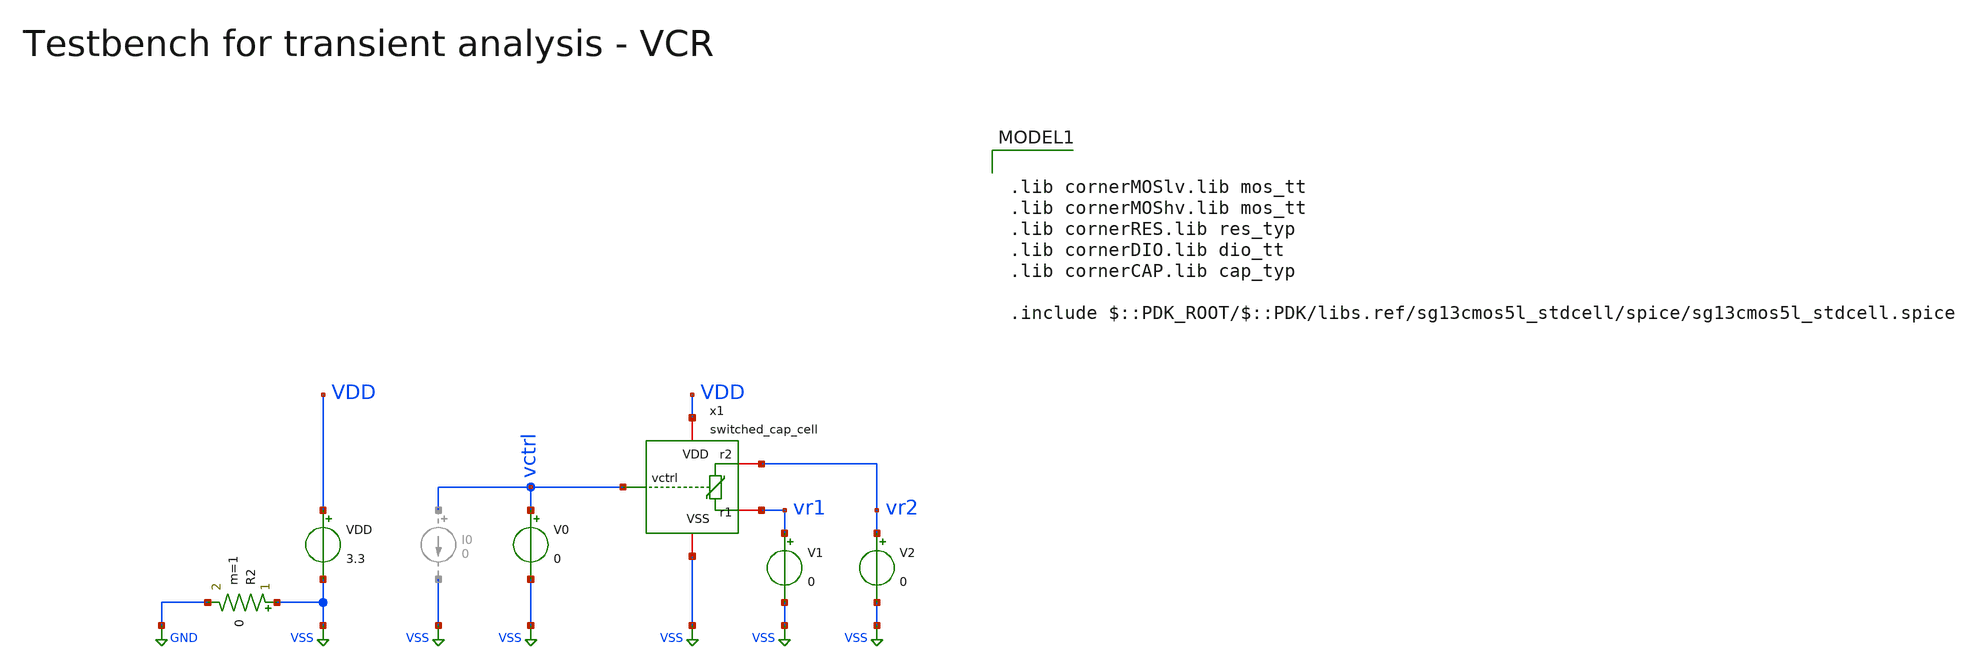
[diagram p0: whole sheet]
** sch_path: macros/heichips26_vcr/macros/switched_capacitor/testbenches/xschem/tb_switched_cap_tran_sweep.sch
**.subckt tb_switched_cap_tran_sweep
VDD VDD VSS 3.3
R2 VSS GND 0 m=1
x1 vctrl VDD VSS vr2 vr1 switched_cap_cell
V1 vr1 VSS 0
V2 vr2 VSS 0
V0 vctrl VSS 0
**** begin user architecture code

.lib cornerMOSlv.lib mos_tt
.lib cornerMOShv.lib mos_tt
.lib cornerRES.lib res_typ
.lib cornerDIO.lib dio_tt
.lib cornerCAP.lib cap_typ

.include $::PDK_ROOT/$::PDK/libs.ref/sg13cmos5l_stdcell/spice/sg13cmos5l_stdcell.spice



.param temp=27

* Derived timing parameters

.options savecurrents klu method=gear reltol=1e-6 abstol=1e-12 gmin=1e-15 noinit
.probe alli
.control

echo
echo # ------------------------------------------------------------------------------
echo # VCM sweep:
echo # ------------------------------------------------------------------------------
echo

unset appendwrite
set wr_vecnames
set wr_singlescale

let vdd_var = 3.3
let record_periods = 2
let v_to_f = 2e6
let vctrl_var = 0.1

set voltages = ( 0.1 0.5 3.3 )
foreach vctrl_var $voltages
	break

	let f = v_to_f/$vctrl_var
	let period = 1/f
	let tstop = record_periods*period
	let tstep = period/100
	echo vctrl=$vctrl_var, f=$&f, period=$&period, tstop=$&tstop, tstep=$&tstep
	alter v0 = $vctrl_var

	let vdm = 1
	let vcm = 0.55
	while vcm < 2.8
		let v1 = $&vcm - $&vdm/2
		let v2 = $&vcm + $&vdm/2
		echo vctrl=$vctrl_var, vcm=$&vcm, vdm=$&vdm, v1=$&v1, v2=$&v2
		alter v1 = $&v1
		alter v2 = $&v2
		tran $&tstep $&tstop
		wrdata ../plot_simulations/data/@schname\_vco_vcm.txt vctrl i(v1) vr1 vr2 x1.clk
		set appendwrite
		unset wr_vecnames
		let vcm = $&vcm + 0.05
	end
end

echo
echo # ------------------------------------------------------------------------------
echo # VDM sweep:
echo # ------------------------------------------------------------------------------
echo

*unset appendwrite
set appendwrite
set wr_vecnames

set voltages = ( 0.1 0.5 3.3 )
foreach vctrl_var $voltages
	let f = v_to_f/$vctrl_var
	let period = 1/f
	let tstop = record_periods*period
	let tstep = period/100
	echo vctrl=$vctrl_var, f=$&f, period=$&period, tstop=$&tstop, tstep=$&tstep
	alter v0 = $vctrl_var

*	let vdm = -$&vdd_var
	let vdm = 2.836
	let vcm = $&vdd_var/2
	while vdm < $&vdd_var
		let v1 = $&vcm - $&vdm/2
		let v2 = $&vcm + $&vdm/2
		echo vctrl=$vctrl_var, vcm=$&vcm, vdm=$&vdm, v1=$&v1, v2=$&v2
		alter v1 = $&v1
		alter v2 = $&v2
		tran $&tstep $&tstop
		wrdata ../plot_simulations/data/@schname\_vco_vdm.txt vctrl i(v1) vr1 vr2 x1.clk
		set appendwrite
		unset wr_vecnames
		let vdm = vdm + 0.052
	end
end

echo
echo # ------------------------------------------------------------------------------
echo # Vctrl sweep:
echo # ------------------------------------------------------------------------------
echo

unset appendwrite
set wr_vecnames

let vdm = $&vdd_var/2
let vcm = $&vdd_var/2
let v1 = $&vcm - $&vdm/2
let v2 = $&vcm + $&vdm/2
echo v1=$&v1, v2=$&v2
alter v1 $&v1
alter v2 $&v2

while $&vctrl_var < 3.4
	let f = v_to_f/$&vctrl_var
	let period = 1/f
	let tstop = record_periods*period
	let tstep = period/100
	echo vctrl=$&vctrl_var, f=$&f, period=$&period, tstop=$&tstop, tstep=$&tstep

	alter v0 = $&vctrl_var
	tran $&tstep $&tstop
	wrdata ../plot_simulations/data/@schname\_vco_vctrl.txt vctrl i(v1) vr1 vr2 x1.clk
	set appendwrite
	unset wr_vecnames
	let vctrl_var = vctrl_var * 1.05
end

*quit
.endc


**** end user architecture code
**.ends

* expanding   symbol:  switched_cap_cell.sym # of pins=5
** sym_path: macros/heichips26_vcr/macros/switched_capacitor/schematic/xschem/switched_cap_cell.sym
** sch_path: macros/heichips26_vcr/macros/switched_capacitor/schematic/xschem/switched_cap_cell.sch
.subckt switched_cap_cell vctrl VDD VSS r2 r1
*.iopin r1
*.iopin r2
*.iopin VDD
*.iopin VSS
*.iopin vctrl
XC1 net1 VSS cap_cmomi w=30e-6 l=30e-6 mmin=1 mmax=4 feed=double subblock=0 m=1 mm_ok=1
x2 net2 net1 r1 net3 VDD VSS transmission_gate
x6 net5 net1 r2 net4 VDD VSS transmission_gate
x3 net2 net3 VDD clk VSS net5 net4 pulse_shaper
x4 net7 VDD clk VSS VSS VSS VSS net6 net8 hv_mux4
x5 VDD net6 VSS net9 vctrl net10 vco
vselA net7 VSS 0
vselB net8 VSS 3.3
.ends


* expanding   symbol:  transmission_gate.sym # of pins=6
** sym_path: macros/heichips26_vcr/macros/switched_capacitor/schematic/xschem/transmission_gate.sym
** sch_path: macros/heichips26_vcr/macros/switched_capacitor/schematic/xschem/transmission_gate.sch
.subckt transmission_gate vctrl vin vout nvctrl VDD VSS
*.iopin vin
*.iopin vout
*.ipin vctrl
*.ipin nvctrl
*.iopin VDD
*.iopin VSS
XM3 vout vctrl vin VSS sg13_hv_nmos w={tg_ngate_w*tg_ng} l={tg_ch_len} ng={tg_ng} m=1 mm_ok=1
XM4 vout nvctrl vin VDD sg13_hv_pmos w={tg_pgate_w*tg_ng} l={tg_ch_len} ng={tg_ng} m=1 mm_ok=1
**** begin user architecture code


.param tg_ch_len=1u
.param tg_ngate_w=2u
.param tg_pgate_w=10u
.param tg_ng=20


**** end user architecture code
.ends


* expanding   symbol:  osc.sym # of pins=6
** sym_path: macros/heichips26_vcr/macros/switched_capacitor/schematic/xschem/osc.sym
** sch_path: macros/heichips26_vcr/macros/switched_capacitor/schematic/xschem/osc.sch
.subckt osc VDD out1 ictrl VSS start out2
*.iopin VSS
*.iopin VDD
*.iopin out2
*.iopin out1
*.iopin start
*.iopin ictrl
XM3 out1 ictrl VDD VDD sg13_hv_pmos w=10.0u l=2.0u ng=1 m=1 mm_ok=1
XM2 net1 ictrl VDD VDD sg13_hv_pmos w=1u l=2.0u ng=1 m=1 mm_ok=1
XM4 start ictrl VDD VDD sg13_hv_pmos w=1.0u l=2.0u ng=1 m=1 mm_ok=1
XM5 out2 ictrl VDD VDD sg13_hv_pmos w=10.0u l=2.0u ng=1 m=1 mm_ok=1
XM6 ictrl ictrl VDD VDD sg13_hv_pmos w=10.0u l=2.0u ng=1 m=1 mm_ok=1
XC1 net1 out1 cap_cmomi w=10e-6 l=10e-6 mmin=1 mmax=4 feed=double subblock=0 m=1 mm_ok=1
XC2 out2 start cap_cmomi w=10e-6 l=10e-6 mmin=1 mmax=4 feed=double subblock=0 m=1 mm_ok=1
XM8 out1 start VSS VSS sg13_hv_nmos w=3u l=0.45u ng=1 m=1 mm_ok=1
XM1 start start VSS VSS sg13_hv_nmos w=1u l=2u ng=1 m=1 mm_ok=1
XM12 out2 net1 VSS VSS sg13_hv_nmos w=3u l=0.45u ng=1 m=1 mm_ok=1
XM11 net1 net1 VSS VSS sg13_hv_nmos w=1u l=2u ng=1 m=1 mm_ok=1
**** begin user architecture code


.ic v(out1)=0 v(out2)=3.3


**** end user architecture code
.ends


* expanding   symbol:  pulse_shaper.sym # of pins=7
** sym_path: macros/heichips26_vcr/macros/switched_capacitor/schematic/xschem/pulse_shaper.sym
** sch_path: macros/heichips26_vcr/macros/switched_capacitor/schematic/xschem/pulse_shaper.sch
.subckt pulse_shaper out1 nout1 VDD in VSS out2 nout2
*.opin out1
*.opin nout1
*.opin out2
*.opin nout2
*.ipin in
*.iopin VSS
*.iopin VDD
x4 VDD net3 nout2 VSS hv_inverter_40u
x7 VDD net1 net3 VSS low_th_inverter
x8 VDD net1 net2 VSS high_th_inverter
x9 VDD net2 out1 VSS hv_inverter_40u
x10 VDD out1 nout1 VSS hv_inverter_40u
x11 VDD nout2 out2 VSS hv_inverter_40u
**** begin user architecture code


.include ../../../netlist/pex/hv_inverter_0u3_magic_pex_3.spice
.param w   = 0.3u
.param ng  = 1
.param n_ng = ng
.param n_w = {w*n_ng}
.param n_l = 0.45u
.param p_ng = ng
.param p_w = {1*w*p_ng}
.param p_l = 0.4u


**** end user architecture code
x1 VDD in net1 VSS hv_inverter_0u3
.ends


* expanding   symbol:  hv_mux4.sym # of pins=9
** sym_path: macros/heichips26_vcr/macros/switched_capacitor/schematic/xschem/hv_mux4.sym
** sch_path: macros/heichips26_vcr/macros/switched_capacitor/schematic/xschem/hv_mux4.sch
.subckt hv_mux4 selA VDD out VSS in3 in1 in4 in2 selB
*.ipin in1
*.iopin VDD
*.iopin VSS
*.opin out
*.ipin in2
*.ipin selA
*.ipin in3
*.ipin in4
*.ipin selB
x3 VDD selA net9 VSS hv_inverter_40u
x1 VDD net2 out net1 VSS net3 net4 hv_nor4
x2 VDD in1 net2 net6 VSS hv_nor
x4 VDD in2 net1 net7 VSS hv_nor
x5 VDD in3 net3 net8 VSS hv_nor
x6 VDD in4 net4 net5 VSS hv_nor
x7 VDD selA net5 selB VSS hv_nand
x9 VDD net9 net7 selB VSS hv_nand
x10 VDD selB net10 VSS hv_inverter_40u
x11 VDD selA net8 net10 VSS hv_nand
x8 VDD net9 net6 net10 VSS hv_nand
.ends


* expanding   symbol:  vco.sym # of pins=6
** sym_path: macros/heichips26_vcr/macros/switched_capacitor/schematic/xschem/vco.sym
** sch_path: macros/heichips26_vcr/macros/switched_capacitor/schematic/xschem/vco.sch
.subckt vco VDD out VSS nout vctrl vc
*.iopin VSS
*.iopin VDD
*.iopin nout
*.iopin out
*.iopin vctrl
*.iopin vc
**** begin user architecture code


.ic v(vc)=1.65


**** end user architecture code
XC1 vc VSS cap_cmomi w=30e-6 l=30e-6 mmin=1 mmax=4 feed=double subblock=0 m=1 mm_ok=1
XM4 vc out 5uA- VSS sg13_hv_nmos w=0.3u l=0.45u ng=1 m=1 mm_ok=1
x1 VDD s out nout r VSS hv_rs-ff
**** begin user architecture code


.param cm_n_w = 6u
.param cm_n_l = 5u
.param cm_p_w = 10u
.param cm_p_l = 2u

.param inv_ng = 1
.param inv_n_w = 2u
.param inv_n_l = 0.45u
.param inv_p_w = 6.5u
.param inv_p_l = 0.4u


**** end user architecture code
XM6 vc out 5uA+ VDD sg13_hv_pmos w=0.3u l=0.4u ng=1 m=1 mm_ok=1
x5 net2 vc vthl VDD 40uA- VSS comp_pmos
x7 net1 vthh vc VDD 40uA+ VSS comp_nmos
x2 10uA- vthl VDD vctrl VSS vthh voltage_mirror_pmos
x3 VDD net1 s VSS hv_inverter_6u5
x6 VDD net2 r VSS hv_inverter_6u5
x8 40uA+ 5uA+ VDD VSS 5uA- 10uA- 40uA- bias_current_generator
.ends


* expanding   symbol:  hv_inverter_40u.sym # of pins=4
** sym_path: macros/heichips26_vcr/macros/switched_capacitor/schematic/xschem/hv_inverter_40u.sym
** sch_path: macros/heichips26_vcr/macros/switched_capacitor/schematic/xschem/hv_inverter_40u.sch
.subckt hv_inverter_40u VDD in out VSS
*.ipin in
*.iopin VDD
*.iopin VSS
*.opin out
XM2 out in VSS VSS sg13_hv_nmos w={n_w} l={n_l} ng={ng} m=1 mm_ok=1
XM3 out in VDD VDD sg13_hv_pmos w={p_w} l={p_l} ng={ng} m=1 mm_ok=1
**** begin user architecture code


.param w   = 10u
.param ng  = 4
.param n_ng = ng
.param n_w = {3u*n_ng}
.param n_l = 0.45u
.param p_ng = ng
.param p_w = {10u*p_ng}
.param p_l = 0.4u


**** end user architecture code
.ends


* expanding   symbol:  low_th_inverter.sym # of pins=4
** sym_path: macros/heichips26_vcr/macros/switched_capacitor/schematic/xschem/low_th_inverter.sym
** sch_path: macros/heichips26_vcr/macros/switched_capacitor/schematic/xschem/low_th_inverter.sch
.subckt low_th_inverter VDD vin vout VSS
*.ipin vin
*.iopin VDD
*.iopin VSS
*.opin vout
XM1 vout vin VSS VSS sg13_hv_nmos w={n_ng*n_w} l={n_l} ng={n_ng} m=1 mm_ok=1
XM2 vout vin VDD VDD sg13_hv_pmos w={p_ng*p_w} l={p_l} ng={n_ng} m=1 mm_ok=1
**** begin user architecture code


.param n_ng = 2
.param n_w = 1u
.param n_l = 0.45u
.param p_ng = 2
.param p_w = 1u
.param p_l = 0.4u


**** end user architecture code
.ends


* expanding   symbol:  high_th_inverter.sym # of pins=4
** sym_path: macros/heichips26_vcr/macros/switched_capacitor/schematic/xschem/high_th_inverter.sym
** sch_path: macros/heichips26_vcr/macros/switched_capacitor/schematic/xschem/high_th_inverter.sch
.subckt high_th_inverter VDD vin vout VSS
*.ipin vin
*.iopin VDD
*.iopin VSS
*.opin vout
XMdummy1 VSS VSS VSS VSS sg13_hv_nmos w=0.6u l=1.0u ng=2 m=1 mm_ok=1
XMdummy2 VDD VDD VDD VDD sg13_hv_pmos w=12.0u l=1.0u ng=2 m=1 mm_ok=1
XM1 vout vin VSS VSS sg13_hv_nmos w=6.0u l=1.0u ng=20 m=1 mm_ok=1
XM2 vout vin VDD VDD sg13_hv_pmos w=120.0u l=1.0u ng=20 m=1 mm_ok=1
.ends


* expanding   symbol:  hv_inverter_0u3.sym # of pins=4
** sym_path: macros/heichips26_vcr/macros/switched_capacitor/schematic/xschem/hv_inverter_0u3.sym
** sch_path: macros/heichips26_vcr/macros/switched_capacitor/schematic/xschem/hv_inverter_0u3.sch
.subckt hv_inverter_0u3 VDD in out VSS
*.ipin in
*.iopin VDD
*.iopin VSS
*.opin out
XM2 out in VSS VSS sg13_hv_nmos w={n_w} l={n_l} ng={ng} m=1 mm_ok=1
XM3 out in VDD VDD sg13_hv_pmos w={p_w} l={p_l} ng={ng} m=1 mm_ok=1
**** begin user architecture code


.param w   = 0.3u
.param ng  = 1
.param n_ng = ng
.param n_w = {w*n_ng}
.param n_l = 0.45u
.param p_ng = ng
.param p_w = {1*w*p_ng}
.param p_l = 0.4u


**** end user architecture code
.ends


* expanding   symbol:  hv_nor4.sym # of pins=7
** sym_path: macros/heichips26_vcr/macros/switched_capacitor/schematic/xschem/hv_nor4.sym
** sch_path: macros/heichips26_vcr/macros/switched_capacitor/schematic/xschem/hv_nor4.sch
.subckt hv_nor4 VDD in1 out in2 VSS in3 in4
*.ipin in1
*.iopin VDD
*.iopin VSS
*.opin out
*.ipin in2
*.ipin in3
*.ipin in4
**** begin user architecture code


.param w   = 10u
.param ng  = 4
.param n_ng = ng
.param n_w = {3u*n_ng}
.param n_l = 0.45u
.param p_ng = ng
.param p_w = {10u*p_ng}
.param p_l = 0.4u


**** end user architecture code
XM2 out in3 VSS VSS sg13_hv_nmos w={n_w} l={n_l} ng={ng} m=1 mm_ok=1
XM3 net3 in4 VDD VDD sg13_hv_pmos w={p_w} l={p_l} ng={ng} m=1 mm_ok=1
XM1 out in4 VSS VSS sg13_hv_nmos w={n_w} l={n_l} ng={ng} m=1 mm_ok=1
XM4 out in1 net1 VDD sg13_hv_pmos w={p_w} l={p_l} ng={ng} m=1 mm_ok=1
XM5 out in2 VSS VSS sg13_hv_nmos w={n_w} l={n_l} ng={ng} m=1 mm_ok=1
XM6 out in1 VSS VSS sg13_hv_nmos w={n_w} l={n_l} ng={ng} m=1 mm_ok=1
XM7 net1 in2 net2 VDD sg13_hv_pmos w={p_w} l={p_l} ng={ng} m=1 mm_ok=1
XM8 net2 in3 net3 VDD sg13_hv_pmos w={p_w} l={p_l} ng={ng} m=1 mm_ok=1
.ends


* expanding   symbol:  hv_nor.sym # of pins=5
** sym_path: macros/heichips26_vcr/macros/switched_capacitor/schematic/xschem/hv_nor.sym
** sch_path: macros/heichips26_vcr/macros/switched_capacitor/schematic/xschem/hv_nor.sch
.subckt hv_nor VDD in1 out in2 VSS
*.ipin in1
*.iopin VDD
*.iopin VSS
*.opin out
*.ipin in2
**** begin user architecture code


.param w   = 10u
.param ng  = 4
.param n_ng = ng
.param n_w = {3u*n_ng}
.param n_l = 0.45u
.param p_ng = ng
.param p_w = {10u*p_ng}
.param p_l = 0.4u


**** end user architecture code
XM2 out in1 VSS VSS sg13_hv_nmos w={n_w} l={n_l} ng={ng} m=1 mm_ok=1
XM3 net1 in2 VDD VDD sg13_hv_pmos w={p_w} l={p_l} ng={ng} m=1 mm_ok=1
XM1 out in2 VSS VSS sg13_hv_nmos w={n_w} l={n_l} ng={ng} m=1 mm_ok=1
XM4 out in1 net1 VDD sg13_hv_pmos w={p_w} l={p_l} ng={ng} m=1 mm_ok=1
.ends


* expanding   symbol:  hv_nand.sym # of pins=5
** sym_path: macros/heichips26_vcr/macros/switched_capacitor/schematic/xschem/hv_nand.sym
** sch_path: macros/heichips26_vcr/macros/switched_capacitor/schematic/xschem/hv_nand.sch
.subckt hv_nand VDD in1 out in2 VSS
*.ipin in1
*.iopin VDD
*.iopin VSS
*.opin out
*.ipin in2
**** begin user architecture code


.param w   = 10u
.param ng  = 4
.param n_ng = ng
.param n_w = {3u*n_ng}
.param n_l = 0.45u
.param p_ng = ng
.param p_w = {10u*p_ng}
.param p_l = 0.4u


**** end user architecture code
XM2 out in1 net1 VSS sg13_hv_nmos w={n_w} l={n_l} ng={ng} m=1 mm_ok=1
XM3 out in2 VDD VDD sg13_hv_pmos w={p_w} l={p_l} ng={ng} m=1 mm_ok=1
XM1 net1 in2 VSS VSS sg13_hv_nmos w={n_w} l={n_l} ng={ng} m=1 mm_ok=1
XM4 out in1 VDD VDD sg13_hv_pmos w={p_w} l={p_l} ng={ng} m=1 mm_ok=1
.ends


* expanding   symbol:  hv_rs-ff.sym # of pins=6
** sym_path: macros/heichips26_vcr/macros/switched_capacitor/schematic/xschem/hv_rs-ff.sym
** sch_path: macros/heichips26_vcr/macros/switched_capacitor/schematic/xschem/hv_rs-ff.sch
.subckt hv_rs-ff VDD nS Q nQ nR VSS
*.ipin nS
*.iopin VDD
*.iopin VSS
*.opin Q
*.ipin nR
*.opin nQ
x4 VDD nS Q nQ VSS hv_nand
x5 VDD Q nQ nR VSS hv_nand
.ends


* expanding   symbol:  comp_pmos.sym # of pins=6
** sym_path: macros/heichips26_vcr/macros/switched_capacitor/schematic/xschem/comp_pmos.sym
** sch_path: macros/heichips26_vcr/macros/switched_capacitor/schematic/xschem/comp_pmos.sch
.subckt comp_pmos out - + VDD Ibias VSS
*.iopin VDD
*.iopin VSS
*.ipin Ibias
*.opin out
*.ipin +
*.ipin -
**** begin user architecture code


.param n_w = 1.2u
.param n_l = 1.5u
.param p_w = 2u
.param p_l = 0.4u
.param bcm = 1


**** end user architecture code
XM9 net1 Ibias VDD VDD sg13_hv_pmos w=bcm*p_w l=p_l ng=1 m=1 mm_ok=1
XM10 out Ibias VDD VDD sg13_hv_pmos w=bcm*p_w l=p_l ng=1 m=1 mm_ok=1
XM11 Ibias Ibias VDD VDD sg13_hv_pmos w=p_w l=p_l ng=1 m=1 mm_ok=1
XM12 net3 + net1 VDD sg13_hv_pmos w=p_w l=p_l ng=1 m=1 mm_ok=1
XM13 net2 - net1 VDD sg13_hv_pmos w=p_w l=p_l ng=1 m=1 mm_ok=1
XM14 net3 net2 VSS VSS sg13_hv_nmos w=n_w l=n_l ng=1 m=1 mm_ok=1
XM15 net2 net2 VSS VSS sg13_hv_nmos w=n_w l=n_l ng=1 m=1 mm_ok=1
XM16 out net3 VSS VSS sg13_hv_nmos w=n_w l=n_l ng=1 m=1 mm_ok=1
.ends


* expanding   symbol:  comp_nmos.sym # of pins=6
** sym_path: macros/heichips26_vcr/macros/switched_capacitor/schematic/xschem/comp_nmos.sym
** sch_path: macros/heichips26_vcr/macros/switched_capacitor/schematic/xschem/comp_nmos.sch
.subckt comp_nmos out - + VDD Ibias VSS
*.iopin VDD
*.iopin VSS
*.ipin -
*.ipin +
*.ipin Ibias
*.opin out
XM8 net2 + net3 VSS sg13_hv_nmos w=n_w l=n_l ng=1 m=1 mm_ok=1
XM6 net1 net1 VDD VDD sg13_hv_pmos w=p_w l=p_l ng=1 m=1 mm_ok=1
XM1 net2 net1 VDD VDD sg13_hv_pmos w=p_w l=p_l ng=1 m=1 mm_ok=1
XM3 net1 - net3 VSS sg13_hv_nmos w=n_w l=n_l ng=1 m=1 mm_ok=1
**** begin user architecture code


.param n_w = 1.2u
.param n_l = 1.5u
.param p_w = 2u
.param p_l = 0.4u


**** end user architecture code
XM2 out net2 VDD VDD sg13_hv_pmos w=p_w l=p_l ng=1 m=1 mm_ok=1
XM4 net3 Ibias VSS VSS sg13_hv_nmos w=2*n_w l=n_l ng=1 m=1 mm_ok=1
XM5 out Ibias VSS VSS sg13_hv_nmos w=2*n_w l=n_l ng=1 m=1 mm_ok=1
XM7 Ibias Ibias VSS VSS sg13_hv_nmos w=n_w l=n_l ng=1 m=1 mm_ok=1
.ends


* expanding   symbol:  voltage_mirror_pmos.sym # of pins=6
** sym_path: macros/heichips26_vcr/macros/switched_capacitor/schematic/xschem/voltage_mirror_pmos.sym
** sch_path: macros/heichips26_vcr/macros/switched_capacitor/schematic/xschem/voltage_mirror_pmos.sch
.subckt voltage_mirror_pmos Ibias nout VDD in VSS out
*.iopin VDD
*.iopin VSS
*.ipin in
*.opin out
*.opin nout
*.ipin Ibias
**** begin user architecture code


.param n_w = 6u
.param n_l = 5u
.param p_w = 10u
.param p_l = 2u


**** end user architecture code
XR1 in Ibias VSS rhigh w=0.5e-6 l=34e-6 m=1 b=0 mm_ok=1
XM4 net1 Ibias VDD VDD sg13_hv_pmos w=p_w l=p_l ng=1 m=1 mm_ok=1
XM5 out net1 VSS VSS sg13_hv_nmos w=n_w l=n_l ng=1 m=1 mm_ok=1
XR2 VSS nout VSS rhigh w=0.5e-6 l=34e-6 m=1 b=0 mm_ok=1
XR3 out VDD VSS rhigh w=0.5e-6 l=34e-6 m=1 b=0 mm_ok=1
XM2 net1 net1 VSS VSS sg13_hv_nmos w=n_w l=n_l ng=1 m=1 mm_ok=1
XM3 nout Ibias VDD VDD sg13_hv_pmos w=p_w l=p_l ng=1 m=1 mm_ok=1
XM6 Ibias Ibias VDD VDD sg13_hv_pmos w=1.9*p_w l=p_l ng=1 m=1 mm_ok=1
.ends


* expanding   symbol:  hv_inverter_6u5.sym # of pins=4
** sym_path: macros/heichips26_vcr/macros/switched_capacitor/schematic/xschem/hv_inverter_6u5.sym
** sch_path: macros/heichips26_vcr/macros/switched_capacitor/schematic/xschem/hv_inverter_6u5.sch
.subckt hv_inverter_6u5 VDD in out VSS
*.ipin in
*.iopin VDD
*.iopin VSS
*.opin out
XM2 out in VSS VSS sg13_hv_nmos w={n_w} l={n_l} ng={ng} m=1 mm_ok=1
XM3 out in VDD VDD sg13_hv_pmos w={p_w} l={p_l} ng={ng} m=1 mm_ok=1
**** begin user architecture code


.param ng  = 1
.param n_ng = ng
.param n_w = {2u*n_ng}
.param n_l = 0.45u
.param p_ng = ng
.param p_w = {6.5u*p_ng}
.param p_l = 0.4u


**** end user architecture code
.ends


* expanding   symbol:  bias_current_generator.sym # of pins=7
** sym_path: macros/heichips26_vcr/macros/switched_capacitor/schematic/xschem/bias_current_generator.sym
** sch_path: macros/heichips26_vcr/macros/switched_capacitor/schematic/xschem/bias_current_generator.sch
.subckt bias_current_generator 40uA+ 5uA+ VDD VSS 5uA- 10uA- 40uA-
*.opin 40uA+
*.iopin VSS
*.iopin VDD
*.opin 40uA-
*.opin 10uA-
*.opin 5uA+
*.opin 5uA-
x4 VDD net1 VSS current_reference_40uA
XM11 net1 net1 VDD VDD sg13_hv_pmos w=cm_p_w l=cm_p_l ng=1 m=1 mm_ok=1
XM12 40uA+ net1 VDD VDD sg13_hv_pmos w=cm_p_w l=cm_p_l ng=1 m=1 mm_ok=1
XM13 net2 net1 VDD VDD sg13_hv_pmos w=cm_p_w l=cm_p_l ng=1 m=1 mm_ok=1
XM14 net2 net2 VSS VSS sg13_hv_nmos w=cm_n_w l=cm_n_l ng=1 m=1 mm_ok=1
XM15 40uA- net2 VSS VSS sg13_hv_nmos w=cm_n_w l=cm_n_l ng=1 m=1 mm_ok=1
XM1 net3 net1 VDD VDD sg13_hv_pmos w=cm_p_w l=cm_p_l ng=1 m=1 mm_ok=1
XM2 net3 net3 VSS VSS sg13_hv_nmos w=4*cm_n_w l=cm_n_l ng=4 m=1 mm_ok=1
XM3 10uA- net3 VSS VSS sg13_hv_nmos w=cm_n_w l=cm_n_l ng=1 m=1 mm_ok=1
XM5 net4 net3 VSS VSS sg13_hv_nmos w=cm_n_w l=cm_n_l ng=1 m=1 mm_ok=1
XM25 net4 net4 VDD VDD sg13_hv_pmos w=2*cm_p_w l=cm_p_l ng=2 m=1 mm_ok=1
XM26 net5 net4 VDD VDD sg13_hv_pmos w=cm_p_w l=cm_p_l ng=1 m=1 mm_ok=1
XM27 5uA+ net4 VDD VDD sg13_hv_pmos w=cm_p_w l=cm_p_l ng=1 m=1 mm_ok=1
XM28 net5 net5 VSS VSS sg13_hv_nmos w=cm_n_w l=cm_n_l ng=2 m=1 mm_ok=1
XM29 5uA- net5 VSS VSS sg13_hv_nmos w=cm_n_w l=cm_n_l ng=1 m=1 mm_ok=1
**** begin user architecture code


.param cm_n_w = 6u
.param cm_n_l = 5u
.param cm_p_w = 10u
.param cm_p_l = 2u


**** end user architecture code
.ends


* expanding   symbol:  current_reference_40uA.sym # of pins=3
** sym_path: macros/heichips26_vcr/macros/switched_capacitor/schematic/xschem/current_reference_40uA.sym
** sch_path: macros/heichips26_vcr/macros/switched_capacitor/schematic/xschem/current_reference_40uA.sch
.subckt current_reference_40uA VDD iout VSS
*.iopin VSS
*.iopin VDD
*.iopin iout
XM8 net2 net2 VSS VSS sg13_hv_nmos w=n_w l=n_l ng=1 m=1 mm_ok=1
XM6 net2 net1 VDD VDD sg13_hv_pmos w=p_w l=p_l ng=1 m=1 mm_ok=1
XM1 net1 net1 VDD VDD sg13_hv_pmos w=p_w l=p_l ng=1 m=1 mm_ok=1
XM3 net1 net2 net3 VSS sg13_hv_nmos w=n_w l=n_l ng=1 m=1 mm_ok=1
XR2 net4 VSS VSS rppd w=2e-6 l=21.9e-6 m=1 b=0 mm_ok=1
XM2 net1 net2 net3 VSS sg13_hv_nmos w=n_w l=n_l ng=1 m=1 mm_ok=1
XM4 net1 net2 net3 VSS sg13_hv_nmos w=n_w l=n_l ng=1 m=1 mm_ok=1
XM5 net1 net2 net3 VSS sg13_hv_nmos w=n_w l=n_l ng=1 m=1 mm_ok=1
XM7 iout net2 VSS VSS sg13_hv_nmos w=n_w l=n_l ng=1 m=1 mm_ok=1
XR3 net3 net4 VSS rsil w=0.5e-6 l=365e-6 m=1 mm_ok=1
**** begin user architecture code


.param n_w = 6u
.param n_l = 5u
.param p_w = 10u
.param p_l = 2u


**** end user architecture code
.ends

.GLOBAL VSS
.GLOBAL GND
.end
